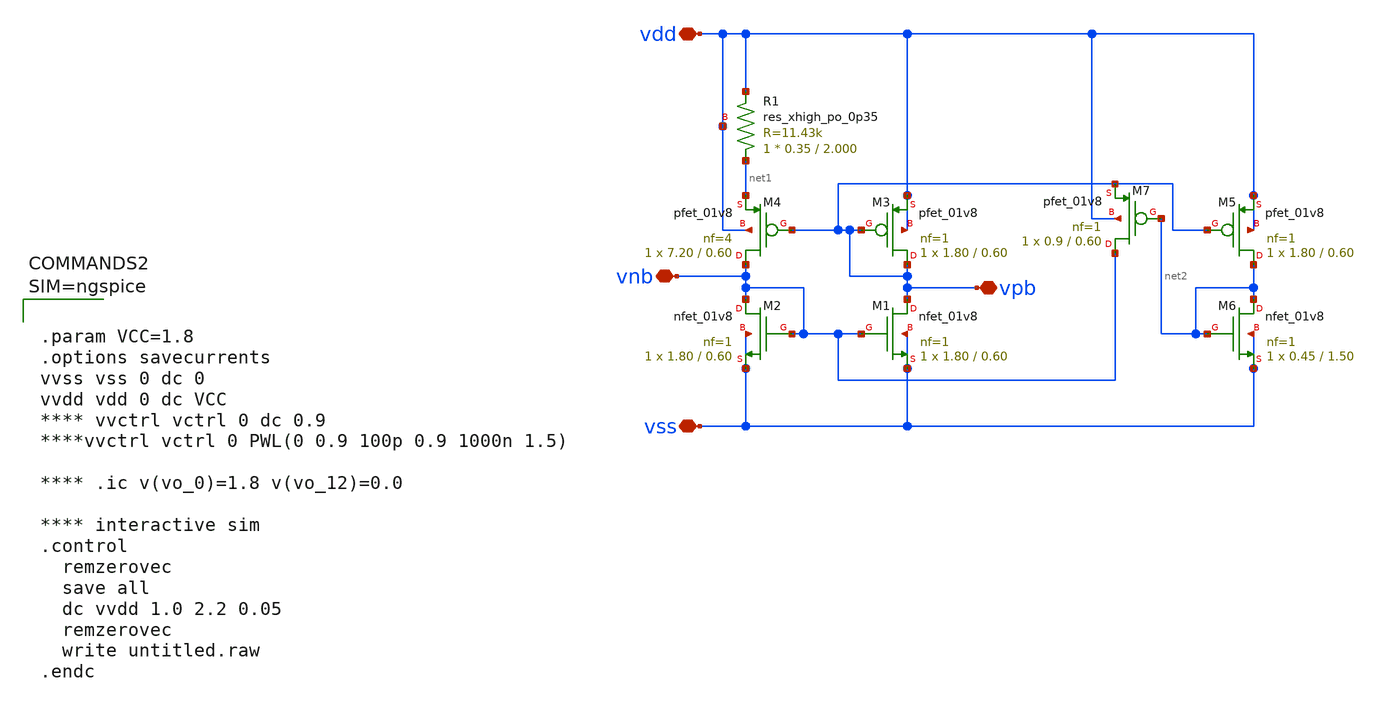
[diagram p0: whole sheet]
** sch_path: custom_gds/tt_um_mickey_pll/xschem/bias.sch
.lib $::SKYWATER_MODELS/sky130.lib.spice tt
.include $::SKYWATER_STDCELLS/sky130_fd_sc_hd.spice

**.subckt bias vdd vss vnb vpb
*.iopin vdd
*.iopin vss
*.iopin vnb
*.iopin vpb
XM1 vpb vnb vss vss sky130_fd_pr__nfet_01v8 L=0.60 W=1.80 nf=1 ad='int((nf+1)/2) * W/nf * 0.29' as='int((nf+2)/2) * W/nf * 0.29'
+ pd='2*int((nf+1)/2) * (W/nf + 0.29)' ps='2*int((nf+2)/2) * (W/nf + 0.29)' nrd='0.29 / W' nrs='0.29 / W'
+ sa=0 sb=0 sd=0 mult=1 m=1
XM2 vnb vnb vss vss sky130_fd_pr__nfet_01v8 L=0.60 W=1.80 nf=1 ad='int((nf+1)/2) * W/nf * 0.29' as='int((nf+2)/2) * W/nf * 0.29'
+ pd='2*int((nf+1)/2) * (W/nf + 0.29)' ps='2*int((nf+2)/2) * (W/nf + 0.29)' nrd='0.29 / W' nrs='0.29 / W'
+ sa=0 sb=0 sd=0 mult=1 m=1
XM3 vpb vpb vdd vdd sky130_fd_pr__pfet_01v8 L=0.60 W=1.80 nf=1 ad='int((nf+1)/2) * W/nf * 0.29' as='int((nf+2)/2) * W/nf * 0.29'
+ pd='2*int((nf+1)/2) * (W/nf + 0.29)' ps='2*int((nf+2)/2) * (W/nf + 0.29)' nrd='0.29 / W' nrs='0.29 / W'
+ sa=0 sb=0 sd=0 mult=1 m=1
XM4 vnb vpb net1 vdd sky130_fd_pr__pfet_01v8 L=0.60 W=7.20 nf=4 ad='int((nf+1)/2) * W/nf * 0.29' as='int((nf+2)/2) * W/nf * 0.29'
+ pd='2*int((nf+1)/2) * (W/nf + 0.29)' ps='2*int((nf+2)/2) * (W/nf + 0.29)' nrd='0.29 / W' nrs='0.29 / W'
+ sa=0 sb=0 sd=0 mult=1 m=1
XM5 net2 vpb vdd vdd sky130_fd_pr__pfet_01v8 L=0.60 W=1.80 nf=1 ad='int((nf+1)/2) * W/nf * 0.29' as='int((nf+2)/2) * W/nf * 0.29'
+ pd='2*int((nf+1)/2) * (W/nf + 0.29)' ps='2*int((nf+2)/2) * (W/nf + 0.29)' nrd='0.29 / W' nrs='0.29 / W'
+ sa=0 sb=0 sd=0 mult=1 m=1
XM6 net2 net2 vss vss sky130_fd_pr__nfet_01v8 L=1.50 W=0.45 nf=1 ad='int((nf+1)/2) * W/nf * 0.29' as='int((nf+2)/2) * W/nf * 0.29'
+ pd='2*int((nf+1)/2) * (W/nf + 0.29)' ps='2*int((nf+2)/2) * (W/nf + 0.29)' nrd='0.29 / W' nrs='0.29 / W'
+ sa=0 sb=0 sd=0 mult=1 m=1
XM7 vnb net2 vpb vdd sky130_fd_pr__pfet_01v8 L=0.60 W=0.9 nf=1 ad='int((nf+1)/2) * W/nf * 0.29' as='int((nf+2)/2) * W/nf * 0.29'
+ pd='2*int((nf+1)/2) * (W/nf + 0.29)' ps='2*int((nf+2)/2) * (W/nf + 0.29)' nrd='0.29 / W' nrs='0.29 / W'
+ sa=0 sb=0 sd=0 mult=1 m=1
XR1 net1 vdd vdd sky130_fd_pr__res_xhigh_po_0p35 L=2.000 mult=1 m=1
**** begin user architecture code



.param VCC=1.8
.options savecurrents
vvss vss 0 dc 0
vvdd vdd 0 dc VCC
**** vvctrl vctrl 0 dc 0.9
****vvctrl vctrl 0 PWL(0 0.9 100p 0.9 1000n 1.5)

**** .ic v(vo_0)=1.8 v(vo_12)=0.0

**** interactive sim
.control
  remzerovec
  save all
  dc vvdd 1.0 2.2 0.05
  remzerovec
  write untitled.raw
.endc



**** end user architecture code
**.ends
.end
